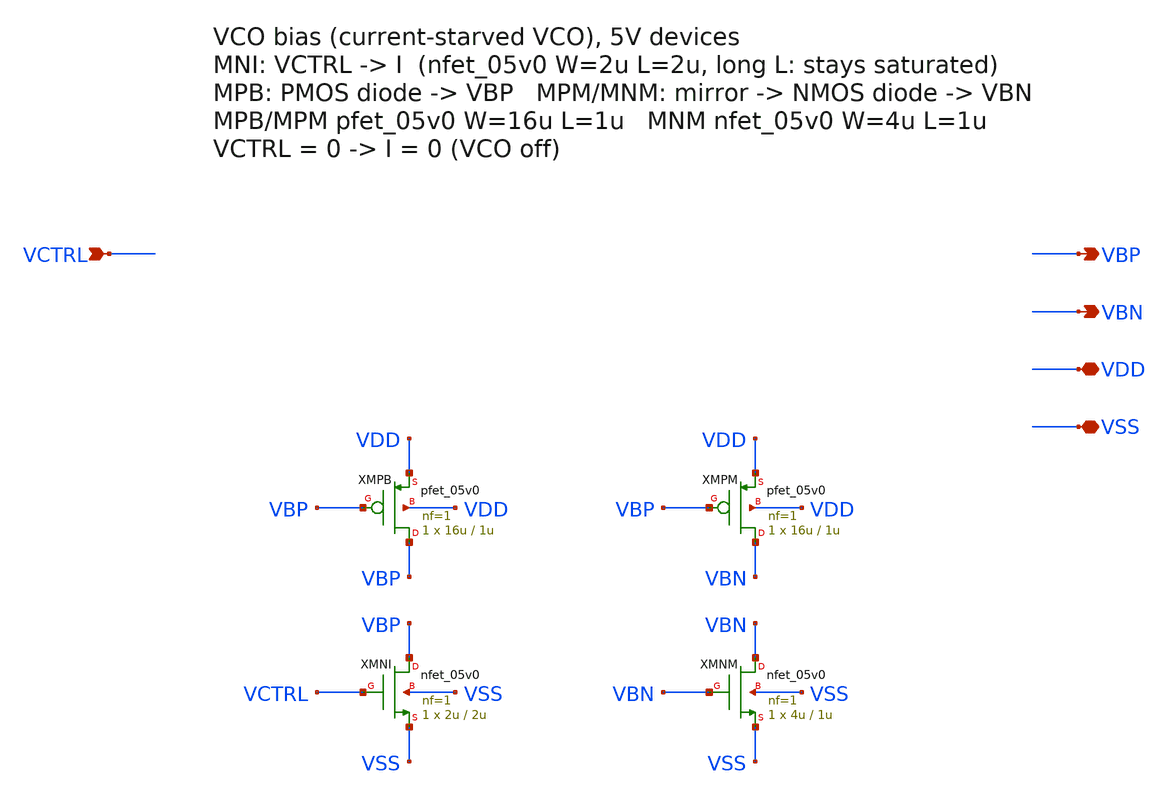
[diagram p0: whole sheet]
** sch_path: vco/vco_bias_5v0.sch
**.subckt vco_bias_5v0 VCTRL VBP VBN VDD VSS
*.ipin VCTRL
*.opin VBP
*.opin VBN
*.iopin VDD
*.iopin VSS
XMPB VBP VBP VDD VDD pfet_05v0 L=1u W=16u nf=1 ad='int((nf+1)/2) * W/nf * 0.18u' as='int((nf+2)/2) * W/nf * 0.18u'
+ pd='2*int((nf+1)/2) * (W/nf + 0.18u)' ps='2*int((nf+2)/2) * (W/nf + 0.18u)' nrd='0.18u / W' nrs='0.18u / W'
+ sa=0 sb=0 sd=0 m=1
XMNI VBP VCTRL VSS VSS nfet_05v0 L=2u W=2u nf=1 ad='int((nf+1)/2) * W/nf * 0.18u' as='int((nf+2)/2) * W/nf * 0.18u'
+ pd='2*int((nf+1)/2) * (W/nf + 0.18u)' ps='2*int((nf+2)/2) * (W/nf + 0.18u)' nrd='0.18u / W' nrs='0.18u / W'
+ sa=0 sb=0 sd=0 m=1
XMPM VBN VBP VDD VDD pfet_05v0 L=1u W=16u nf=1 ad='int((nf+1)/2) * W/nf * 0.18u' as='int((nf+2)/2) * W/nf * 0.18u'
+ pd='2*int((nf+1)/2) * (W/nf + 0.18u)' ps='2*int((nf+2)/2) * (W/nf + 0.18u)' nrd='0.18u / W' nrs='0.18u / W'
+ sa=0 sb=0 sd=0 m=1
XMNM VBN VBN VSS VSS nfet_05v0 L=1u W=4u nf=1 ad='int((nf+1)/2) * W/nf * 0.18u' as='int((nf+2)/2) * W/nf * 0.18u'
+ pd='2*int((nf+1)/2) * (W/nf + 0.18u)' ps='2*int((nf+2)/2) * (W/nf + 0.18u)' nrd='0.18u / W' nrs='0.18u / W'
+ sa=0 sb=0 sd=0 m=1
**.ends
.end
